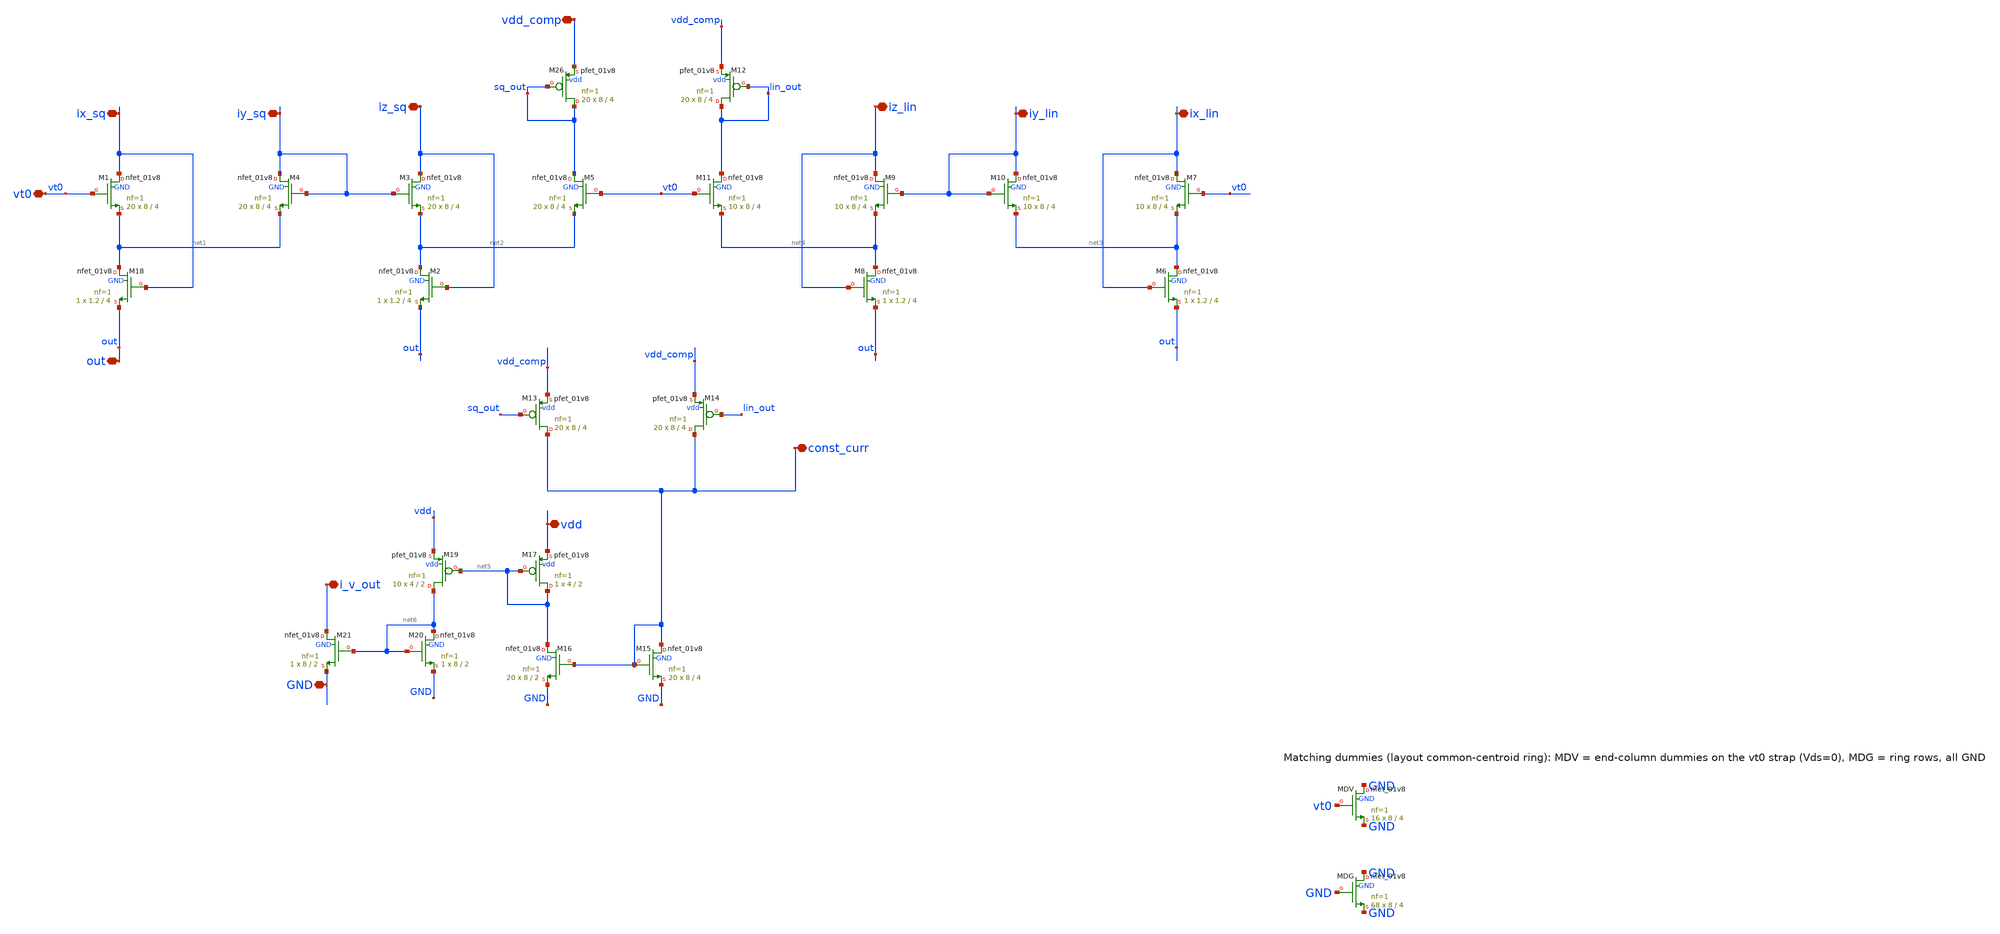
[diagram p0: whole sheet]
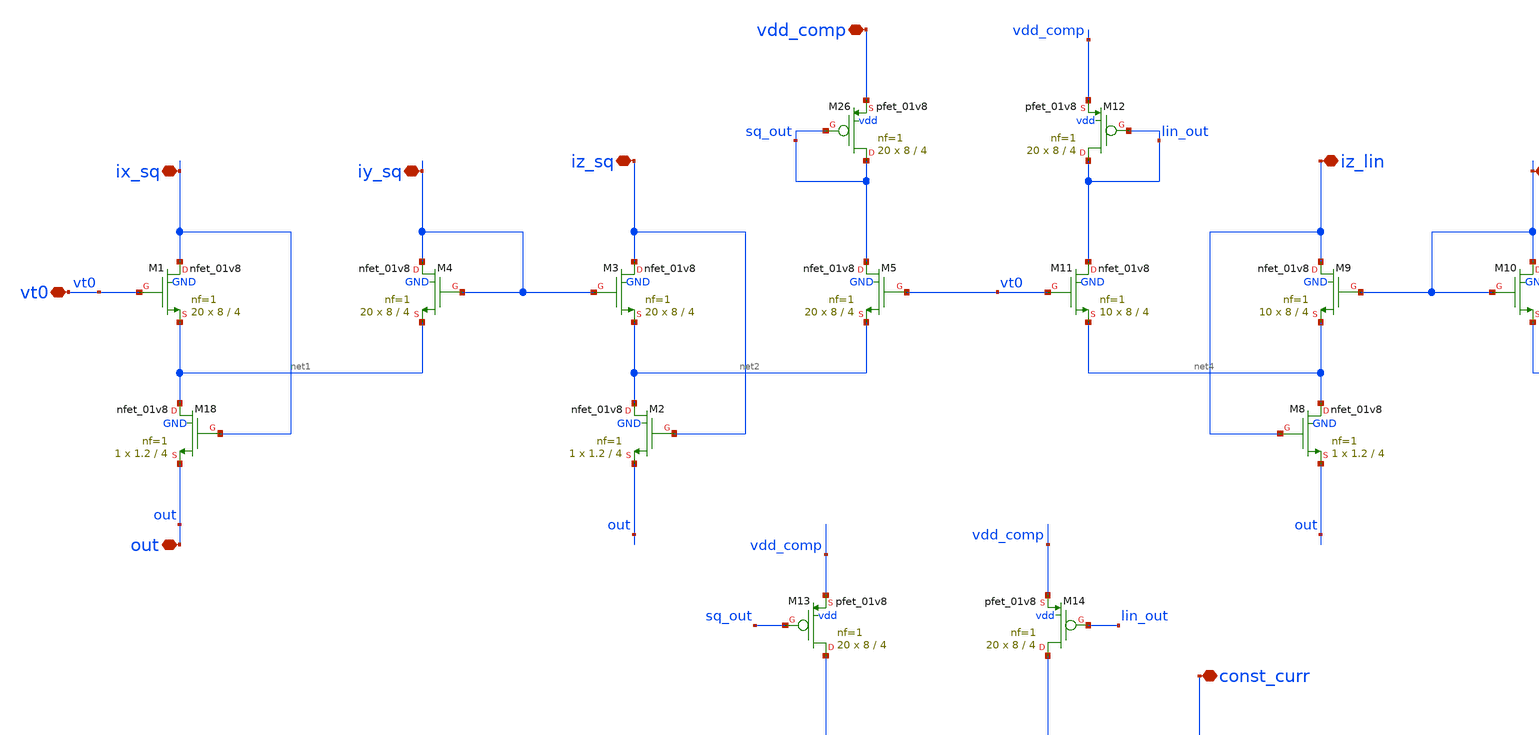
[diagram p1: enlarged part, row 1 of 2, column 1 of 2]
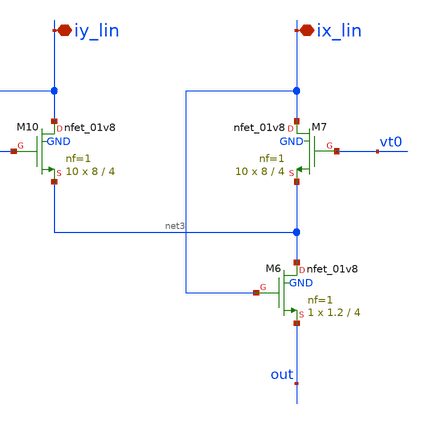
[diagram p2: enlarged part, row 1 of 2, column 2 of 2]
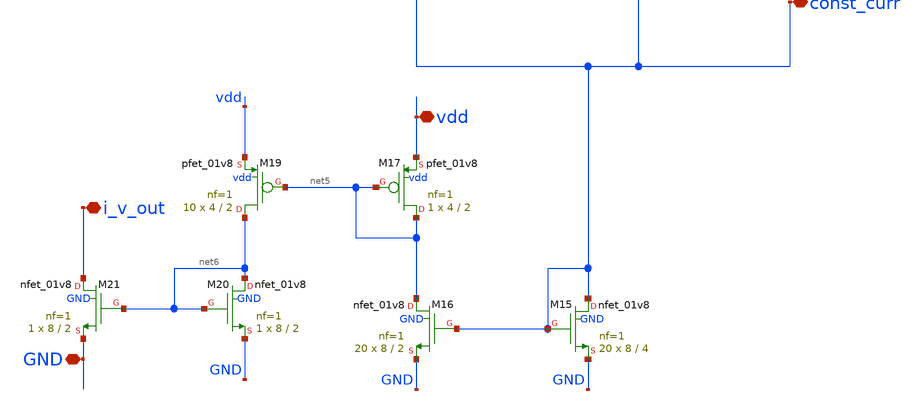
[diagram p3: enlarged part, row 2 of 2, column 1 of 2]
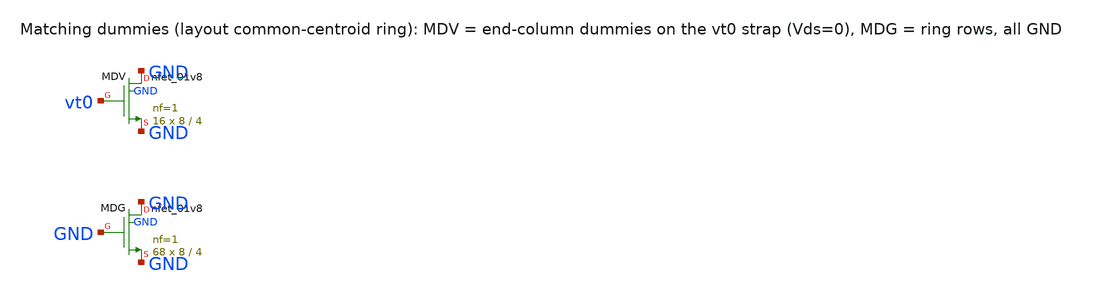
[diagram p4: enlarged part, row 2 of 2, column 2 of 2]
** sch_path: xschem/blocks/combined.sch
**.subckt combined vt0 ix_sq iy_sq iz_sq vdd_comp ix_lin iy_lin iz_lin out const_curr i_v_out vdd
*+ GND
*.iopin vt0
*.iopin ix_sq
*.iopin iy_sq
*.iopin iz_sq
*.iopin vdd_comp
*.iopin ix_lin
*.iopin iy_lin
*.iopin iz_lin
*.iopin out
*.iopin const_curr
*.iopin i_v_out
*.iopin vdd
*.iopin GND
XM18 net1 ix_sq out GND sky130_fd_pr__nfet_01v8 L=4 W=1.2 nf=1 ad='int((nf+1)/2) * W/nf * 0.29' as='int((nf+2)/2) * W/nf * 0.29'
+ pd='2*int((nf+1)/2) * (W/nf + 0.29)' ps='2*int((nf+2)/2) * (W/nf + 0.29)' nrd='0.29 / W' nrs='0.29 / W'
+ sa=0 sb=0 sd=0 mult=1 m=1
XM1 ix_sq vt0 net1 GND sky130_fd_pr__nfet_01v8 L=4 W=8 nf=1 ad='int((nf+1)/2) * W/nf * 0.29' as='int((nf+2)/2) * W/nf * 0.29'
+ pd='2*int((nf+1)/2) * (W/nf + 0.29)' ps='2*int((nf+2)/2) * (W/nf + 0.29)' nrd='0.29 / W' nrs='0.29 / W'
+ sa=0 sb=0 sd=0 mult=20 m=20
XM2 net2 iz_sq out GND sky130_fd_pr__nfet_01v8 L=4 W=1.2 nf=1 ad='int((nf+1)/2) * W/nf * 0.29' as='int((nf+2)/2) * W/nf * 0.29'
+ pd='2*int((nf+1)/2) * (W/nf + 0.29)' ps='2*int((nf+2)/2) * (W/nf + 0.29)' nrd='0.29 / W' nrs='0.29 / W'
+ sa=0 sb=0 sd=0 mult=1 m=1
XM3 iz_sq iy_sq net2 GND sky130_fd_pr__nfet_01v8 L=4 W=8 nf=1 ad='int((nf+1)/2) * W/nf * 0.29' as='int((nf+2)/2) * W/nf * 0.29'
+ pd='2*int((nf+1)/2) * (W/nf + 0.29)' ps='2*int((nf+2)/2) * (W/nf + 0.29)' nrd='0.29 / W' nrs='0.29 / W'
+ sa=0 sb=0 sd=0 mult=20 m=20
XM4 iy_sq iy_sq net1 GND sky130_fd_pr__nfet_01v8 L=4 W=8 nf=1 ad='int((nf+1)/2) * W/nf * 0.29' as='int((nf+2)/2) * W/nf * 0.29'
+ pd='2*int((nf+1)/2) * (W/nf + 0.29)' ps='2*int((nf+2)/2) * (W/nf + 0.29)' nrd='0.29 / W' nrs='0.29 / W'
+ sa=0 sb=0 sd=0 mult=20 m=20
XM5 sq_out vt0 net2 GND sky130_fd_pr__nfet_01v8 L=4 W=8 nf=1 ad='int((nf+1)/2) * W/nf * 0.29' as='int((nf+2)/2) * W/nf * 0.29'
+ pd='2*int((nf+1)/2) * (W/nf + 0.29)' ps='2*int((nf+2)/2) * (W/nf + 0.29)' nrd='0.29 / W' nrs='0.29 / W'
+ sa=0 sb=0 sd=0 mult=20 m=20
XM26 sq_out sq_out vdd_comp vdd sky130_fd_pr__pfet_01v8 L=4 W=8 nf=1 ad='int((1 + 1)/2) * 8 / 1 * 0.29'
+ as='int((1 + 2)/2) * 8 / 1 * 0.29' pd='2*int((1 + 1)/2) * (8 / 1 + 0.29)' ps='2*int((1 + 2)/2) * (8 / 1 + 0.29)'
+ nrd='0.29 / 8 ' nrs='0.29 / 8 ' sa=0 sb=0 sd=0 mult=20 m=20
XM6 net3 ix_lin out GND sky130_fd_pr__nfet_01v8 L=4 W=1.2 nf=1 ad='int((nf+1)/2) * W/nf * 0.29' as='int((nf+2)/2) * W/nf * 0.29'
+ pd='2*int((nf+1)/2) * (W/nf + 0.29)' ps='2*int((nf+2)/2) * (W/nf + 0.29)' nrd='0.29 / W' nrs='0.29 / W'
+ sa=0 sb=0 sd=0 mult=1 m=1
XM7 ix_lin vt0 net3 GND sky130_fd_pr__nfet_01v8 L=4 W=8 nf=1 ad='int((nf+1)/2) * W/nf * 0.29' as='int((nf+2)/2) * W/nf * 0.29'
+ pd='2*int((nf+1)/2) * (W/nf + 0.29)' ps='2*int((nf+2)/2) * (W/nf + 0.29)' nrd='0.29 / W' nrs='0.29 / W'
+ sa=0 sb=0 sd=0 mult=10 m=10
XM8 net4 iz_lin out GND sky130_fd_pr__nfet_01v8 L=4 W=1.2 nf=1 ad='int((nf+1)/2) * W/nf * 0.29' as='int((nf+2)/2) * W/nf * 0.29'
+ pd='2*int((nf+1)/2) * (W/nf + 0.29)' ps='2*int((nf+2)/2) * (W/nf + 0.29)' nrd='0.29 / W' nrs='0.29 / W'
+ sa=0 sb=0 sd=0 mult=1 m=1
XM9 iz_lin iy_lin net4 GND sky130_fd_pr__nfet_01v8 L=4 W=8 nf=1 ad='int((nf+1)/2) * W/nf * 0.29' as='int((nf+2)/2) * W/nf * 0.29'
+ pd='2*int((nf+1)/2) * (W/nf + 0.29)' ps='2*int((nf+2)/2) * (W/nf + 0.29)' nrd='0.29 / W' nrs='0.29 / W'
+ sa=0 sb=0 sd=0 mult=10 m=10
XM10 iy_lin iy_lin net3 GND sky130_fd_pr__nfet_01v8 L=4 W=8 nf=1 ad='int((nf+1)/2) * W/nf * 0.29' as='int((nf+2)/2) * W/nf * 0.29'
+ pd='2*int((nf+1)/2) * (W/nf + 0.29)' ps='2*int((nf+2)/2) * (W/nf + 0.29)' nrd='0.29 / W' nrs='0.29 / W'
+ sa=0 sb=0 sd=0 mult=10 m=10
XM11 lin_out vt0 net4 GND sky130_fd_pr__nfet_01v8 L=4 W=8 nf=1 ad='int((nf+1)/2) * W/nf * 0.29' as='int((nf+2)/2) * W/nf * 0.29'
+ pd='2*int((nf+1)/2) * (W/nf + 0.29)' ps='2*int((nf+2)/2) * (W/nf + 0.29)' nrd='0.29 / W' nrs='0.29 / W'
+ sa=0 sb=0 sd=0 mult=10 m=10
XM12 lin_out lin_out vdd_comp vdd sky130_fd_pr__pfet_01v8 L=4 W=8 nf=1 ad='int((1 + 1)/2) * 8 / 1 * 0.29'
+ as='int((1 + 2)/2) * 8 / 1 * 0.29' pd='2*int((1 + 1)/2) * (8 / 1 + 0.29)' ps='2*int((1 + 2)/2) * (8 / 1 + 0.29)'
+ nrd='0.29 / 8 ' nrs='0.29 / 8 ' sa=0 sb=0 sd=0 mult=20 m=20
XM13 const_curr sq_out vdd_comp vdd sky130_fd_pr__pfet_01v8 L=4 W=8 nf=1 ad='int((1 + 1)/2) * 8 / 1 * 0.29'
+ as='int((1 + 2)/2) * 8 / 1 * 0.29' pd='2*int((1 + 1)/2) * (8 / 1 + 0.29)' ps='2*int((1 + 2)/2) * (8 / 1 + 0.29)'
+ nrd='0.29 / 8 ' nrs='0.29 / 8 ' sa=0 sb=0 sd=0 mult=20 m=20
XM14 const_curr lin_out vdd_comp vdd sky130_fd_pr__pfet_01v8 L=4 W=8 nf=1 ad='int((1 + 1)/2) * 8 / 1 * 0.29'
+ as='int((1 + 2)/2) * 8 / 1 * 0.29' pd='2*int((1 + 1)/2) * (8 / 1 + 0.29)' ps='2*int((1 + 2)/2) * (8 / 1 + 0.29)'
+ nrd='0.29 / 8 ' nrs='0.29 / 8 ' sa=0 sb=0 sd=0 mult=20 m=20
XM15 const_curr const_curr GND GND sky130_fd_pr__nfet_01v8 L=4 W=8 nf=1 ad='int((nf+1)/2) * W/nf * 0.29'
+ as='int((nf+2)/2) * W/nf * 0.29' pd='2*int((nf+1)/2) * (W/nf + 0.29)' ps='2*int((nf+2)/2) * (W/nf + 0.29)'
+ nrd='0.29 / W' nrs='0.29 / W' sa=0 sb=0 sd=0 mult=20 m=20
XM16 net5 const_curr GND GND sky130_fd_pr__nfet_01v8 L=2 W=8 nf=1 ad='int((nf+1)/2) * W/nf * 0.29' as='int((nf+2)/2) * W/nf * 0.29'
+ pd='2*int((nf+1)/2) * (W/nf + 0.29)' ps='2*int((nf+2)/2) * (W/nf + 0.29)' nrd='0.29 / W' nrs='0.29 / W'
+ sa=0 sb=0 sd=0 mult=20 m=20
XM17 net5 net5 vdd vdd sky130_fd_pr__pfet_01v8 L=2 W=4 nf=1 ad='int((1 + 1)/2) * 4 / 1 * 0.29' as='int((1 + 2)/2) * 4 / 1 * 0.29'
+ pd='2*int((1 + 1)/2) * (4 / 1 + 0.29)' ps='2*int((1 + 2)/2) * (4 / 1 + 0.29)' nrd='0.29 / 4 ' nrs='0.29 / 4 '
+ sa=0 sb=0 sd=0 mult=1 m=1
XM19 net6 net5 vdd vdd sky130_fd_pr__pfet_01v8 L=2 W=4 nf=1 ad='int((1 + 1)/2) * 4 / 1 * 0.29' as='int((1 + 2)/2) * 4 / 1 * 0.29'
+ pd='2*int((1 + 1)/2) * (4 / 1 + 0.29)' ps='2*int((1 + 2)/2) * (4 / 1 + 0.29)' nrd='0.29 / 4 ' nrs='0.29 / 4 '
+ sa=0 sb=0 sd=0 mult=10 m=10
XM20 net6 net6 GND GND sky130_fd_pr__nfet_01v8 L=2 W=8 nf=1 ad='int((nf+1)/2) * W/nf * 0.29' as='int((nf+2)/2) * W/nf * 0.29'
+ pd='2*int((nf+1)/2) * (W/nf + 0.29)' ps='2*int((nf+2)/2) * (W/nf + 0.29)' nrd='0.29 / W' nrs='0.29 / W'
+ sa=0 sb=0 sd=0 mult=1 m=1
XM21 i_v_out net6 GND GND sky130_fd_pr__nfet_01v8 L=2 W=8 nf=1 ad='int((nf+1)/2) * W/nf * 0.29' as='int((nf+2)/2) * W/nf * 0.29'
+ pd='2*int((nf+1)/2) * (W/nf + 0.29)' ps='2*int((nf+2)/2) * (W/nf + 0.29)' nrd='0.29 / W' nrs='0.29 / W'
+ sa=0 sb=0 sd=0 mult=1 m=1
XMDV GND vt0 GND GND sky130_fd_pr__nfet_01v8 L=4 W=8 nf=1 ad='int((nf+1)/2) * W/nf * 0.29' as='int((nf+2)/2) * W/nf * 0.29'
+ pd='2*int((nf+1)/2) * (W/nf + 0.29)' ps='2*int((nf+2)/2) * (W/nf + 0.29)' nrd='0.29 / W' nrs='0.29 / W'
+ sa=0 sb=0 sd=0 mult=16 m=16
XMDG GND GND GND GND sky130_fd_pr__nfet_01v8 L=4 W=8 nf=1 ad='int((nf+1)/2) * W/nf * 0.29' as='int((nf+2)/2) * W/nf * 0.29'
+ pd='2*int((nf+1)/2) * (W/nf + 0.29)' ps='2*int((nf+2)/2) * (W/nf + 0.29)' nrd='0.29 / W' nrs='0.29 / W'
+ sa=0 sb=0 sd=0 mult=68 m=68
**.ends
.end
